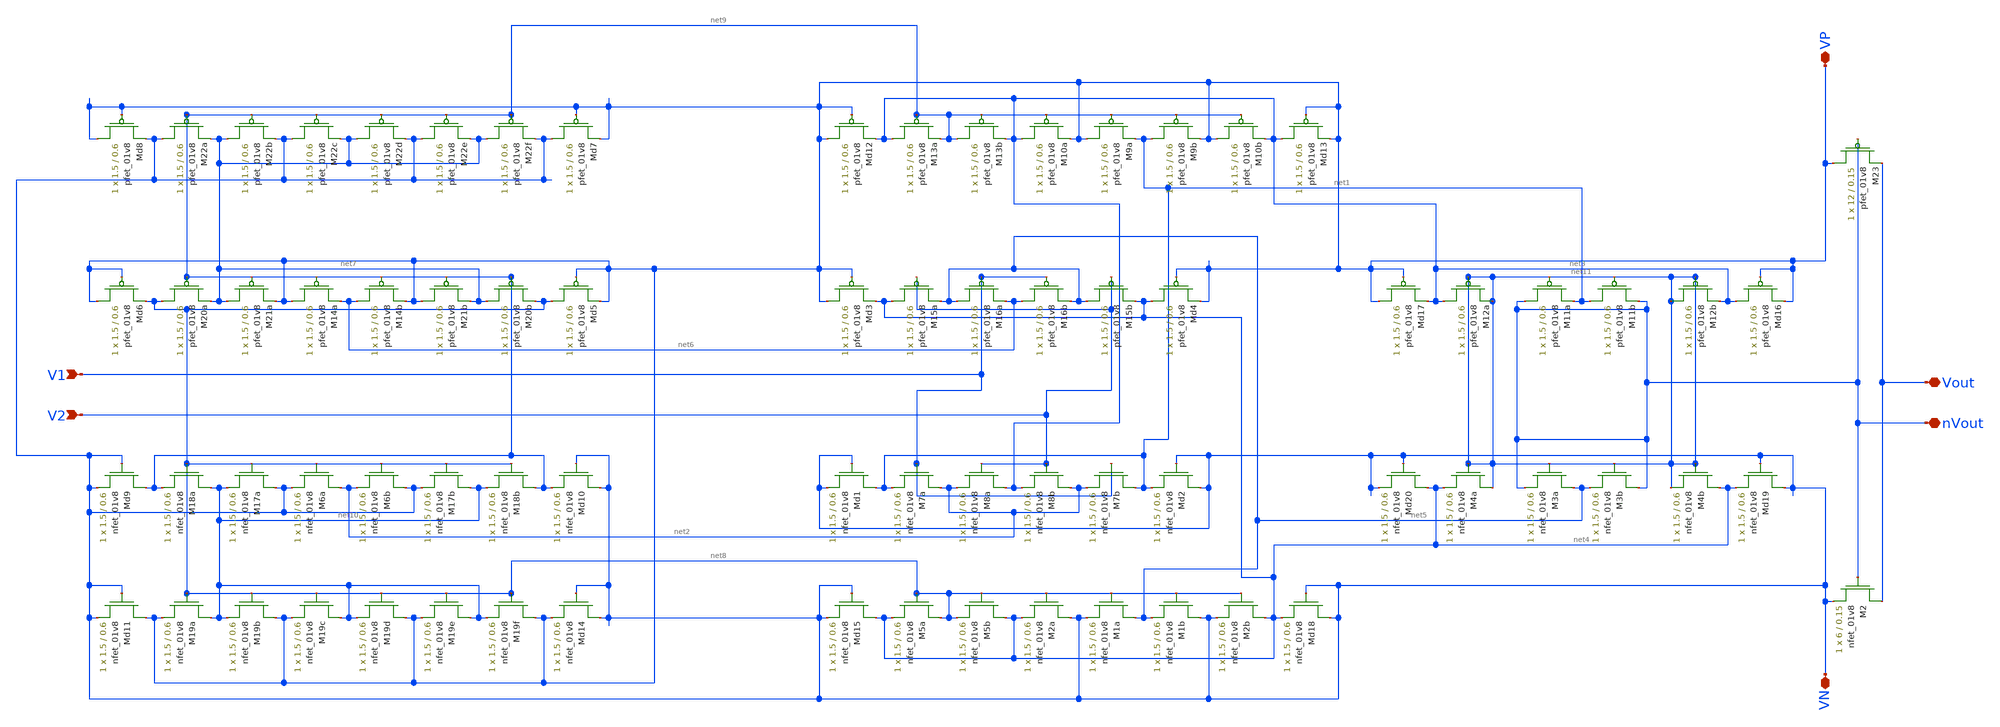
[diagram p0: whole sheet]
** sch_path: analog/sbc2.sch
**.subckt sbc2 V1 V2 Vout nVout VP VN
*.ipin V1
*.ipin V2
*.iopin Vout
*.iopin nVout
*.iopin VP
*.iopin VN
XM7a net2 V1 net1 GND sky130_fd_pr__nfet_01v8 L=0.6 W=1.5 nf=1 ad='int((nf+1)/2) * W/nf * 0.29' as='int((nf+2)/2) * W/nf * 0.29'
+ pd='2*int((nf+1)/2) * (W/nf + 0.29)' ps='2*int((nf+2)/2) * (W/nf + 0.29)' nrd='0.29 / W' nrs='0.29 / W'
+ sa=0 sb=0 sd=0 mult=1 m=1
XM8a net3 V2 net2 GND sky130_fd_pr__nfet_01v8 L=0.6 W=1.5 nf=1 ad='int((nf+1)/2) * W/nf * 0.29' as='int((nf+2)/2) * W/nf * 0.29'
+ pd='2*int((nf+1)/2) * (W/nf + 0.29)' ps='2*int((nf+2)/2) * (W/nf + 0.29)' nrd='0.29 / W' nrs='0.29 / W'
+ sa=0 sb=0 sd=0 mult=1 m=1
XM8b net2 V2 net3 GND sky130_fd_pr__nfet_01v8 L=0.6 W=1.5 nf=1 ad='int((nf+1)/2) * W/nf * 0.29' as='int((nf+2)/2) * W/nf * 0.29'
+ pd='2*int((nf+1)/2) * (W/nf + 0.29)' ps='2*int((nf+2)/2) * (W/nf + 0.29)' nrd='0.29 / W' nrs='0.29 / W'
+ sa=0 sb=0 sd=0 mult=1 m=1
XM7b net1 V1 net2 GND sky130_fd_pr__nfet_01v8 L=0.6 W=1.5 nf=1 ad='int((nf+1)/2) * W/nf * 0.29' as='int((nf+2)/2) * W/nf * 0.29'
+ pd='2*int((nf+1)/2) * (W/nf + 0.29)' ps='2*int((nf+2)/2) * (W/nf + 0.29)' nrd='0.29 / W' nrs='0.29 / W'
+ sa=0 sb=0 sd=0 mult=1 m=1
XMd1 net1 VN VN GND sky130_fd_pr__nfet_01v8 L=0.6 W=1.5 nf=1 ad='int((nf+1)/2) * W/nf * 0.29' as='int((nf+2)/2) * W/nf * 0.29'
+ pd='2*int((nf+1)/2) * (W/nf + 0.29)' ps='2*int((nf+2)/2) * (W/nf + 0.29)' nrd='0.29 / W' nrs='0.29 / W'
+ sa=0 sb=0 sd=0 mult=1 m=1
XMd2 VN VN net1 GND sky130_fd_pr__nfet_01v8 L=0.6 W=1.5 nf=1 ad='int((nf+1)/2) * W/nf * 0.29' as='int((nf+2)/2) * W/nf * 0.29'
+ pd='2*int((nf+1)/2) * (W/nf + 0.29)' ps='2*int((nf+2)/2) * (W/nf + 0.29)' nrd='0.29 / W' nrs='0.29 / W'
+ sa=0 sb=0 sd=0 mult=1 m=1
XMd3 VP VP net4 VDD sky130_fd_pr__pfet_01v8 L=0.6 W=1.5 nf=1 ad='int((nf+1)/2) * W/nf * 0.29' as='int((nf+2)/2) * W/nf * 0.29'
+ pd='2*int((nf+1)/2) * (W/nf + 0.29)' ps='2*int((nf+2)/2) * (W/nf + 0.29)' nrd='0.29 / W' nrs='0.29 / W'
+ sa=0 sb=0 sd=0 mult=1 m=1
XM15a net4 V2 net5 VDD sky130_fd_pr__pfet_01v8 L=0.6 W=1.5 nf=1 ad='int((nf+1)/2) * W/nf * 0.29' as='int((nf+2)/2) * W/nf * 0.29'
+ pd='2*int((nf+1)/2) * (W/nf + 0.29)' ps='2*int((nf+2)/2) * (W/nf + 0.29)' nrd='0.29 / W' nrs='0.29 / W'
+ sa=0 sb=0 sd=0 mult=1 m=1
XM16a net5 V1 net6 VDD sky130_fd_pr__pfet_01v8 L=0.6 W=1.5 nf=1 ad='int((nf+1)/2) * W/nf * 0.29' as='int((nf+2)/2) * W/nf * 0.29'
+ pd='2*int((nf+1)/2) * (W/nf + 0.29)' ps='2*int((nf+2)/2) * (W/nf + 0.29)' nrd='0.29 / W' nrs='0.29 / W'
+ sa=0 sb=0 sd=0 mult=1 m=1
XM16b net6 V1 net5 VDD sky130_fd_pr__pfet_01v8 L=0.6 W=1.5 nf=1 ad='int((nf+1)/2) * W/nf * 0.29' as='int((nf+2)/2) * W/nf * 0.29'
+ pd='2*int((nf+1)/2) * (W/nf + 0.29)' ps='2*int((nf+2)/2) * (W/nf + 0.29)' nrd='0.29 / W' nrs='0.29 / W'
+ sa=0 sb=0 sd=0 mult=1 m=1
XM15b net5 V2 net4 VDD sky130_fd_pr__pfet_01v8 L=0.6 W=1.5 nf=1 ad='int((nf+1)/2) * W/nf * 0.29' as='int((nf+2)/2) * W/nf * 0.29'
+ pd='2*int((nf+1)/2) * (W/nf + 0.29)' ps='2*int((nf+2)/2) * (W/nf + 0.29)' nrd='0.29 / W' nrs='0.29 / W'
+ sa=0 sb=0 sd=0 mult=1 m=1
XMd4 net4 VP VP VDD sky130_fd_pr__pfet_01v8 L=0.6 W=1.5 nf=1 ad='int((nf+1)/2) * W/nf * 0.29' as='int((nf+2)/2) * W/nf * 0.29'
+ pd='2*int((nf+1)/2) * (W/nf + 0.29)' ps='2*int((nf+2)/2) * (W/nf + 0.29)' nrd='0.29 / W' nrs='0.29 / W'
+ sa=0 sb=0 sd=0 mult=1 m=1
XM20a net8 net9 net7 VDD sky130_fd_pr__pfet_01v8 L=0.6 W=1.5 nf=1 ad='int((nf+1)/2) * W/nf * 0.29' as='int((nf+2)/2) * W/nf * 0.29'
+ pd='2*int((nf+1)/2) * (W/nf + 0.29)' ps='2*int((nf+2)/2) * (W/nf + 0.29)' nrd='0.29 / W' nrs='0.29 / W'
+ sa=0 sb=0 sd=0 mult=1 m=1
XM21a net7 net9 VP VDD sky130_fd_pr__pfet_01v8 L=0.6 W=1.5 nf=1 ad='int((nf+1)/2) * W/nf * 0.29' as='int((nf+2)/2) * W/nf * 0.29'
+ pd='2*int((nf+1)/2) * (W/nf + 0.29)' ps='2*int((nf+2)/2) * (W/nf + 0.29)' nrd='0.29 / W' nrs='0.29 / W'
+ sa=0 sb=0 sd=0 mult=1 m=1
XM14a VP net9 net6 VDD sky130_fd_pr__pfet_01v8 L=0.6 W=1.5 nf=1 ad='int((nf+1)/2) * W/nf * 0.29' as='int((nf+2)/2) * W/nf * 0.29'
+ pd='2*int((nf+1)/2) * (W/nf + 0.29)' ps='2*int((nf+2)/2) * (W/nf + 0.29)' nrd='0.29 / W' nrs='0.29 / W'
+ sa=0 sb=0 sd=0 mult=1 m=1
XM14b net6 net9 VP VDD sky130_fd_pr__pfet_01v8 L=0.6 W=1.5 nf=1 ad='int((nf+1)/2) * W/nf * 0.29' as='int((nf+2)/2) * W/nf * 0.29'
+ pd='2*int((nf+1)/2) * (W/nf + 0.29)' ps='2*int((nf+2)/2) * (W/nf + 0.29)' nrd='0.29 / W' nrs='0.29 / W'
+ sa=0 sb=0 sd=0 mult=1 m=1
XM21b VP net9 net7 VDD sky130_fd_pr__pfet_01v8 L=0.6 W=1.5 nf=1 ad='int((nf+1)/2) * W/nf * 0.29' as='int((nf+2)/2) * W/nf * 0.29'
+ pd='2*int((nf+1)/2) * (W/nf + 0.29)' ps='2*int((nf+2)/2) * (W/nf + 0.29)' nrd='0.29 / W' nrs='0.29 / W'
+ sa=0 sb=0 sd=0 mult=1 m=1
XM20b net7 net9 net8 VDD sky130_fd_pr__pfet_01v8 L=0.6 W=1.5 nf=1 ad='int((nf+1)/2) * W/nf * 0.29' as='int((nf+2)/2) * W/nf * 0.29'
+ pd='2*int((nf+1)/2) * (W/nf + 0.29)' ps='2*int((nf+2)/2) * (W/nf + 0.29)' nrd='0.29 / W' nrs='0.29 / W'
+ sa=0 sb=0 sd=0 mult=1 m=1
XMd5 net8 VP VP VDD sky130_fd_pr__pfet_01v8 L=0.6 W=1.5 nf=1 ad='int((nf+1)/2) * W/nf * 0.29' as='int((nf+2)/2) * W/nf * 0.29'
+ pd='2*int((nf+1)/2) * (W/nf + 0.29)' ps='2*int((nf+2)/2) * (W/nf + 0.29)' nrd='0.29 / W' nrs='0.29 / W'
+ sa=0 sb=0 sd=0 mult=1 m=1
XMd6 VP VP net8 VDD sky130_fd_pr__pfet_01v8 L=0.6 W=1.5 nf=1 ad='int((nf+1)/2) * W/nf * 0.29' as='int((nf+2)/2) * W/nf * 0.29'
+ pd='2*int((nf+1)/2) * (W/nf + 0.29)' ps='2*int((nf+2)/2) * (W/nf + 0.29)' nrd='0.29 / W' nrs='0.29 / W'
+ sa=0 sb=0 sd=0 mult=1 m=1
XM22a VN net9 net7 VDD sky130_fd_pr__pfet_01v8 L=0.6 W=1.5 nf=1 ad='int((nf+1)/2) * W/nf * 0.29' as='int((nf+2)/2) * W/nf * 0.29'
+ pd='2*int((nf+1)/2) * (W/nf + 0.29)' ps='2*int((nf+2)/2) * (W/nf + 0.29)' nrd='0.29 / W' nrs='0.29 / W'
+ sa=0 sb=0 sd=0 mult=1 m=1
XM22b net7 net9 VN VDD sky130_fd_pr__pfet_01v8 L=0.6 W=1.5 nf=1 ad='int((nf+1)/2) * W/nf * 0.29' as='int((nf+2)/2) * W/nf * 0.29'
+ pd='2*int((nf+1)/2) * (W/nf + 0.29)' ps='2*int((nf+2)/2) * (W/nf + 0.29)' nrd='0.29 / W' nrs='0.29 / W'
+ sa=0 sb=0 sd=0 mult=1 m=1
XM22c VN net9 net7 VDD sky130_fd_pr__pfet_01v8 L=0.6 W=1.5 nf=1 ad='int((nf+1)/2) * W/nf * 0.29' as='int((nf+2)/2) * W/nf * 0.29'
+ pd='2*int((nf+1)/2) * (W/nf + 0.29)' ps='2*int((nf+2)/2) * (W/nf + 0.29)' nrd='0.29 / W' nrs='0.29 / W'
+ sa=0 sb=0 sd=0 mult=1 m=1
XM22d net7 net9 VN VDD sky130_fd_pr__pfet_01v8 L=0.6 W=1.5 nf=1 ad='int((nf+1)/2) * W/nf * 0.29' as='int((nf+2)/2) * W/nf * 0.29'
+ pd='2*int((nf+1)/2) * (W/nf + 0.29)' ps='2*int((nf+2)/2) * (W/nf + 0.29)' nrd='0.29 / W' nrs='0.29 / W'
+ sa=0 sb=0 sd=0 mult=1 m=1
XM22e VN net9 net7 VDD sky130_fd_pr__pfet_01v8 L=0.6 W=1.5 nf=1 ad='int((nf+1)/2) * W/nf * 0.29' as='int((nf+2)/2) * W/nf * 0.29'
+ pd='2*int((nf+1)/2) * (W/nf + 0.29)' ps='2*int((nf+2)/2) * (W/nf + 0.29)' nrd='0.29 / W' nrs='0.29 / W'
+ sa=0 sb=0 sd=0 mult=1 m=1
XM22f net7 net9 VN VDD sky130_fd_pr__pfet_01v8 L=0.6 W=1.5 nf=1 ad='int((nf+1)/2) * W/nf * 0.29' as='int((nf+2)/2) * W/nf * 0.29'
+ pd='2*int((nf+1)/2) * (W/nf + 0.29)' ps='2*int((nf+2)/2) * (W/nf + 0.29)' nrd='0.29 / W' nrs='0.29 / W'
+ sa=0 sb=0 sd=0 mult=1 m=1
XMd7 VN VP VP VDD sky130_fd_pr__pfet_01v8 L=0.6 W=1.5 nf=1 ad='int((nf+1)/2) * W/nf * 0.29' as='int((nf+2)/2) * W/nf * 0.29'
+ pd='2*int((nf+1)/2) * (W/nf + 0.29)' ps='2*int((nf+2)/2) * (W/nf + 0.29)' nrd='0.29 / W' nrs='0.29 / W'
+ sa=0 sb=0 sd=0 mult=1 m=1
XMd8 VP VP VN VDD sky130_fd_pr__pfet_01v8 L=0.6 W=1.5 nf=1 ad='int((nf+1)/2) * W/nf * 0.29' as='int((nf+2)/2) * W/nf * 0.29'
+ pd='2*int((nf+1)/2) * (W/nf + 0.29)' ps='2*int((nf+2)/2) * (W/nf + 0.29)' nrd='0.29 / W' nrs='0.29 / W'
+ sa=0 sb=0 sd=0 mult=1 m=1
XM18a net10 net8 net9 GND sky130_fd_pr__nfet_01v8 L=0.6 W=1.5 nf=1 ad='int((nf+1)/2) * W/nf * 0.29' as='int((nf+2)/2) * W/nf * 0.29'
+ pd='2*int((nf+1)/2) * (W/nf + 0.29)' ps='2*int((nf+2)/2) * (W/nf + 0.29)' nrd='0.29 / W' nrs='0.29 / W'
+ sa=0 sb=0 sd=0 mult=1 m=1
XM17a VN net8 net10 GND sky130_fd_pr__nfet_01v8 L=0.6 W=1.5 nf=1 ad='int((nf+1)/2) * W/nf * 0.29' as='int((nf+2)/2) * W/nf * 0.29'
+ pd='2*int((nf+1)/2) * (W/nf + 0.29)' ps='2*int((nf+2)/2) * (W/nf + 0.29)' nrd='0.29 / W' nrs='0.29 / W'
+ sa=0 sb=0 sd=0 mult=1 m=1
XM6a net2 net8 VN GND sky130_fd_pr__nfet_01v8 L=0.6 W=1.5 nf=1 ad='int((nf+1)/2) * W/nf * 0.29' as='int((nf+2)/2) * W/nf * 0.29'
+ pd='2*int((nf+1)/2) * (W/nf + 0.29)' ps='2*int((nf+2)/2) * (W/nf + 0.29)' nrd='0.29 / W' nrs='0.29 / W'
+ sa=0 sb=0 sd=0 mult=1 m=1
XM6b VN net8 net2 GND sky130_fd_pr__nfet_01v8 L=0.6 W=1.5 nf=1 ad='int((nf+1)/2) * W/nf * 0.29' as='int((nf+2)/2) * W/nf * 0.29'
+ pd='2*int((nf+1)/2) * (W/nf + 0.29)' ps='2*int((nf+2)/2) * (W/nf + 0.29)' nrd='0.29 / W' nrs='0.29 / W'
+ sa=0 sb=0 sd=0 mult=1 m=1
XMd9 net9 VN VN GND sky130_fd_pr__nfet_01v8 L=0.6 W=1.5 nf=1 ad='int((nf+1)/2) * W/nf * 0.29' as='int((nf+2)/2) * W/nf * 0.29'
+ pd='2*int((nf+1)/2) * (W/nf + 0.29)' ps='2*int((nf+2)/2) * (W/nf + 0.29)' nrd='0.29 / W' nrs='0.29 / W'
+ sa=0 sb=0 sd=0 mult=1 m=1
XM17b net10 net8 VN GND sky130_fd_pr__nfet_01v8 L=0.6 W=1.5 nf=1 ad='int((nf+1)/2) * W/nf * 0.29' as='int((nf+2)/2) * W/nf * 0.29'
+ pd='2*int((nf+1)/2) * (W/nf + 0.29)' ps='2*int((nf+2)/2) * (W/nf + 0.29)' nrd='0.29 / W' nrs='0.29 / W'
+ sa=0 sb=0 sd=0 mult=1 m=1
XM18b net9 net8 net10 GND sky130_fd_pr__nfet_01v8 L=0.6 W=1.5 nf=1 ad='int((nf+1)/2) * W/nf * 0.29' as='int((nf+2)/2) * W/nf * 0.29'
+ pd='2*int((nf+1)/2) * (W/nf + 0.29)' ps='2*int((nf+2)/2) * (W/nf + 0.29)' nrd='0.29 / W' nrs='0.29 / W'
+ sa=0 sb=0 sd=0 mult=1 m=1
XMd10 VN VN net9 GND sky130_fd_pr__nfet_01v8 L=0.6 W=1.5 nf=1 ad='int((nf+1)/2) * W/nf * 0.29' as='int((nf+2)/2) * W/nf * 0.29'
+ pd='2*int((nf+1)/2) * (W/nf + 0.29)' ps='2*int((nf+2)/2) * (W/nf + 0.29)' nrd='0.29 / W' nrs='0.29 / W'
+ sa=0 sb=0 sd=0 mult=1 m=1
XM19a net10 net8 VP GND sky130_fd_pr__nfet_01v8 L=0.6 W=1.5 nf=1 ad='int((nf+1)/2) * W/nf * 0.29' as='int((nf+2)/2) * W/nf * 0.29'
+ pd='2*int((nf+1)/2) * (W/nf + 0.29)' ps='2*int((nf+2)/2) * (W/nf + 0.29)' nrd='0.29 / W' nrs='0.29 / W'
+ sa=0 sb=0 sd=0 mult=1 m=1
XM19b VP net8 net10 GND sky130_fd_pr__nfet_01v8 L=0.6 W=1.5 nf=1 ad='int((nf+1)/2) * W/nf * 0.29' as='int((nf+2)/2) * W/nf * 0.29'
+ pd='2*int((nf+1)/2) * (W/nf + 0.29)' ps='2*int((nf+2)/2) * (W/nf + 0.29)' nrd='0.29 / W' nrs='0.29 / W'
+ sa=0 sb=0 sd=0 mult=1 m=1
XM19c net10 net8 VP GND sky130_fd_pr__nfet_01v8 L=0.6 W=1.5 nf=1 ad='int((nf+1)/2) * W/nf * 0.29' as='int((nf+2)/2) * W/nf * 0.29'
+ pd='2*int((nf+1)/2) * (W/nf + 0.29)' ps='2*int((nf+2)/2) * (W/nf + 0.29)' nrd='0.29 / W' nrs='0.29 / W'
+ sa=0 sb=0 sd=0 mult=1 m=1
XM19d VP net8 net10 GND sky130_fd_pr__nfet_01v8 L=0.6 W=1.5 nf=1 ad='int((nf+1)/2) * W/nf * 0.29' as='int((nf+2)/2) * W/nf * 0.29'
+ pd='2*int((nf+1)/2) * (W/nf + 0.29)' ps='2*int((nf+2)/2) * (W/nf + 0.29)' nrd='0.29 / W' nrs='0.29 / W'
+ sa=0 sb=0 sd=0 mult=1 m=1
XMd11 VP VN VN GND sky130_fd_pr__nfet_01v8 L=0.6 W=1.5 nf=1 ad='int((nf+1)/2) * W/nf * 0.29' as='int((nf+2)/2) * W/nf * 0.29'
+ pd='2*int((nf+1)/2) * (W/nf + 0.29)' ps='2*int((nf+2)/2) * (W/nf + 0.29)' nrd='0.29 / W' nrs='0.29 / W'
+ sa=0 sb=0 sd=0 mult=1 m=1
XM19e net10 net8 VP GND sky130_fd_pr__nfet_01v8 L=0.6 W=1.5 nf=1 ad='int((nf+1)/2) * W/nf * 0.29' as='int((nf+2)/2) * W/nf * 0.29'
+ pd='2*int((nf+1)/2) * (W/nf + 0.29)' ps='2*int((nf+2)/2) * (W/nf + 0.29)' nrd='0.29 / W' nrs='0.29 / W'
+ sa=0 sb=0 sd=0 mult=1 m=1
XM19f VP net8 net10 GND sky130_fd_pr__nfet_01v8 L=0.6 W=1.5 nf=1 ad='int((nf+1)/2) * W/nf * 0.29' as='int((nf+2)/2) * W/nf * 0.29'
+ pd='2*int((nf+1)/2) * (W/nf + 0.29)' ps='2*int((nf+2)/2) * (W/nf + 0.29)' nrd='0.29 / W' nrs='0.29 / W'
+ sa=0 sb=0 sd=0 mult=1 m=1
XMd14 VN VN VP GND sky130_fd_pr__nfet_01v8 L=0.6 W=1.5 nf=1 ad='int((nf+1)/2) * W/nf * 0.29' as='int((nf+2)/2) * W/nf * 0.29'
+ pd='2*int((nf+1)/2) * (W/nf + 0.29)' ps='2*int((nf+2)/2) * (W/nf + 0.29)' nrd='0.29 / W' nrs='0.29 / W'
+ sa=0 sb=0 sd=0 mult=1 m=1
XM13a net3 net9 net9 VDD sky130_fd_pr__pfet_01v8 L=0.6 W=1.5 nf=1 ad='int((nf+1)/2) * W/nf * 0.29' as='int((nf+2)/2) * W/nf * 0.29'
+ pd='2*int((nf+1)/2) * (W/nf + 0.29)' ps='2*int((nf+2)/2) * (W/nf + 0.29)' nrd='0.29 / W' nrs='0.29 / W'
+ sa=0 sb=0 sd=0 mult=1 m=1
XM13b net9 net9 net3 VDD sky130_fd_pr__pfet_01v8 L=0.6 W=1.5 nf=1 ad='int((nf+1)/2) * W/nf * 0.29' as='int((nf+2)/2) * W/nf * 0.29'
+ pd='2*int((nf+1)/2) * (W/nf + 0.29)' ps='2*int((nf+2)/2) * (W/nf + 0.29)' nrd='0.29 / W' nrs='0.29 / W'
+ sa=0 sb=0 sd=0 mult=1 m=1
XM10a net3 net9 VP VDD sky130_fd_pr__pfet_01v8 L=0.6 W=1.5 nf=1 ad='int((nf+1)/2) * W/nf * 0.29' as='int((nf+2)/2) * W/nf * 0.29'
+ pd='2*int((nf+1)/2) * (W/nf + 0.29)' ps='2*int((nf+2)/2) * (W/nf + 0.29)' nrd='0.29 / W' nrs='0.29 / W'
+ sa=0 sb=0 sd=0 mult=1 m=1
XM9a VP net9 net1 VDD sky130_fd_pr__pfet_01v8 L=0.6 W=1.5 nf=1 ad='int((nf+1)/2) * W/nf * 0.29' as='int((nf+2)/2) * W/nf * 0.29'
+ pd='2*int((nf+1)/2) * (W/nf + 0.29)' ps='2*int((nf+2)/2) * (W/nf + 0.29)' nrd='0.29 / W' nrs='0.29 / W'
+ sa=0 sb=0 sd=0 mult=1 m=1
XM9b net1 net9 VP VDD sky130_fd_pr__pfet_01v8 L=0.6 W=1.5 nf=1 ad='int((nf+1)/2) * W/nf * 0.29' as='int((nf+2)/2) * W/nf * 0.29'
+ pd='2*int((nf+1)/2) * (W/nf + 0.29)' ps='2*int((nf+2)/2) * (W/nf + 0.29)' nrd='0.29 / W' nrs='0.29 / W'
+ sa=0 sb=0 sd=0 mult=1 m=1
XM10b VP net9 net3 VDD sky130_fd_pr__pfet_01v8 L=0.6 W=1.5 nf=1 ad='int((nf+1)/2) * W/nf * 0.29' as='int((nf+2)/2) * W/nf * 0.29'
+ pd='2*int((nf+1)/2) * (W/nf + 0.29)' ps='2*int((nf+2)/2) * (W/nf + 0.29)' nrd='0.29 / W' nrs='0.29 / W'
+ sa=0 sb=0 sd=0 mult=1 m=1
XMd12 VP VP net3 VDD sky130_fd_pr__pfet_01v8 L=0.6 W=1.5 nf=1 ad='int((nf+1)/2) * W/nf * 0.29' as='int((nf+2)/2) * W/nf * 0.29'
+ pd='2*int((nf+1)/2) * (W/nf + 0.29)' ps='2*int((nf+2)/2) * (W/nf + 0.29)' nrd='0.29 / W' nrs='0.29 / W'
+ sa=0 sb=0 sd=0 mult=1 m=1
XMd13 net3 VP VP VDD sky130_fd_pr__pfet_01v8 L=0.6 W=1.5 nf=1 ad='int((nf+1)/2) * W/nf * 0.29' as='int((nf+2)/2) * W/nf * 0.29'
+ pd='2*int((nf+1)/2) * (W/nf + 0.29)' ps='2*int((nf+2)/2) * (W/nf + 0.29)' nrd='0.29 / W' nrs='0.29 / W'
+ sa=0 sb=0 sd=0 mult=1 m=1
XM5a net8 net8 net4 GND sky130_fd_pr__nfet_01v8 L=0.6 W=1.5 nf=1 ad='int((nf+1)/2) * W/nf * 0.29' as='int((nf+2)/2) * W/nf * 0.29'
+ pd='2*int((nf+1)/2) * (W/nf + 0.29)' ps='2*int((nf+2)/2) * (W/nf + 0.29)' nrd='0.29 / W' nrs='0.29 / W'
+ sa=0 sb=0 sd=0 mult=1 m=1
XM5b net4 net8 net8 GND sky130_fd_pr__nfet_01v8 L=0.6 W=1.5 nf=1 ad='int((nf+1)/2) * W/nf * 0.29' as='int((nf+2)/2) * W/nf * 0.29'
+ pd='2*int((nf+1)/2) * (W/nf + 0.29)' ps='2*int((nf+2)/2) * (W/nf + 0.29)' nrd='0.29 / W' nrs='0.29 / W'
+ sa=0 sb=0 sd=0 mult=1 m=1
XM2a VN net8 net4 GND sky130_fd_pr__nfet_01v8 L=0.6 W=1.5 nf=1 ad='int((nf+1)/2) * W/nf * 0.29' as='int((nf+2)/2) * W/nf * 0.29'
+ pd='2*int((nf+1)/2) * (W/nf + 0.29)' ps='2*int((nf+2)/2) * (W/nf + 0.29)' nrd='0.29 / W' nrs='0.29 / W'
+ sa=0 sb=0 sd=0 mult=1 m=1
XM1a net5 net8 VN GND sky130_fd_pr__nfet_01v8 L=0.6 W=1.5 nf=1 ad='int((nf+1)/2) * W/nf * 0.29' as='int((nf+2)/2) * W/nf * 0.29'
+ pd='2*int((nf+1)/2) * (W/nf + 0.29)' ps='2*int((nf+2)/2) * (W/nf + 0.29)' nrd='0.29 / W' nrs='0.29 / W'
+ sa=0 sb=0 sd=0 mult=1 m=1
XMd15 net4 VN VN GND sky130_fd_pr__nfet_01v8 L=0.6 W=1.5 nf=1 ad='int((nf+1)/2) * W/nf * 0.29' as='int((nf+2)/2) * W/nf * 0.29'
+ pd='2*int((nf+1)/2) * (W/nf + 0.29)' ps='2*int((nf+2)/2) * (W/nf + 0.29)' nrd='0.29 / W' nrs='0.29 / W'
+ sa=0 sb=0 sd=0 mult=1 m=1
XM1b VN net8 net5 GND sky130_fd_pr__nfet_01v8 L=0.6 W=1.5 nf=1 ad='int((nf+1)/2) * W/nf * 0.29' as='int((nf+2)/2) * W/nf * 0.29'
+ pd='2*int((nf+1)/2) * (W/nf + 0.29)' ps='2*int((nf+2)/2) * (W/nf + 0.29)' nrd='0.29 / W' nrs='0.29 / W'
+ sa=0 sb=0 sd=0 mult=1 m=1
XM2b net4 net8 VN GND sky130_fd_pr__nfet_01v8 L=0.6 W=1.5 nf=1 ad='int((nf+1)/2) * W/nf * 0.29' as='int((nf+2)/2) * W/nf * 0.29'
+ pd='2*int((nf+1)/2) * (W/nf + 0.29)' ps='2*int((nf+2)/2) * (W/nf + 0.29)' nrd='0.29 / W' nrs='0.29 / W'
+ sa=0 sb=0 sd=0 mult=1 m=1
XMd18 VN VN net4 GND sky130_fd_pr__nfet_01v8 L=0.6 W=1.5 nf=1 ad='int((nf+1)/2) * W/nf * 0.29' as='int((nf+2)/2) * W/nf * 0.29'
+ pd='2*int((nf+1)/2) * (W/nf + 0.29)' ps='2*int((nf+2)/2) * (W/nf + 0.29)' nrd='0.29 / W' nrs='0.29 / W'
+ sa=0 sb=0 sd=0 mult=1 m=1
XM12a net3 net11 net11 VDD sky130_fd_pr__pfet_01v8 L=0.6 W=1.5 nf=1 ad='int((nf+1)/2) * W/nf * 0.29'
+ as='int((nf+2)/2) * W/nf * 0.29' pd='2*int((nf+1)/2) * (W/nf + 0.29)' ps='2*int((nf+2)/2) * (W/nf + 0.29)'
+ nrd='0.29 / W' nrs='0.29 / W' sa=0 sb=0 sd=0 mult=1 m=1
XM11a nVout net11 net1 VDD sky130_fd_pr__pfet_01v8 L=0.6 W=1.5 nf=1 ad='int((nf+1)/2) * W/nf * 0.29'
+ as='int((nf+2)/2) * W/nf * 0.29' pd='2*int((nf+1)/2) * (W/nf + 0.29)' ps='2*int((nf+2)/2) * (W/nf + 0.29)'
+ nrd='0.29 / W' nrs='0.29 / W' sa=0 sb=0 sd=0 mult=1 m=1
XM11b net1 net11 nVout VDD sky130_fd_pr__pfet_01v8 L=0.6 W=1.5 nf=1 ad='int((nf+1)/2) * W/nf * 0.29'
+ as='int((nf+2)/2) * W/nf * 0.29' pd='2*int((nf+1)/2) * (W/nf + 0.29)' ps='2*int((nf+2)/2) * (W/nf + 0.29)'
+ nrd='0.29 / W' nrs='0.29 / W' sa=0 sb=0 sd=0 mult=1 m=1
XM12b net11 net11 net3 VDD sky130_fd_pr__pfet_01v8 L=0.6 W=1.5 nf=1 ad='int((nf+1)/2) * W/nf * 0.29'
+ as='int((nf+2)/2) * W/nf * 0.29' pd='2*int((nf+1)/2) * (W/nf + 0.29)' ps='2*int((nf+2)/2) * (W/nf + 0.29)'
+ nrd='0.29 / W' nrs='0.29 / W' sa=0 sb=0 sd=0 mult=1 m=1
XMd16 net3 VP VP VDD sky130_fd_pr__pfet_01v8 L=0.6 W=1.5 nf=1 ad='int((nf+1)/2) * W/nf * 0.29' as='int((nf+2)/2) * W/nf * 0.29'
+ pd='2*int((nf+1)/2) * (W/nf + 0.29)' ps='2*int((nf+2)/2) * (W/nf + 0.29)' nrd='0.29 / W' nrs='0.29 / W'
+ sa=0 sb=0 sd=0 mult=1 m=1
XMd17 VP VP net3 VDD sky130_fd_pr__pfet_01v8 L=0.6 W=1.5 nf=1 ad='int((nf+1)/2) * W/nf * 0.29' as='int((nf+2)/2) * W/nf * 0.29'
+ pd='2*int((nf+1)/2) * (W/nf + 0.29)' ps='2*int((nf+2)/2) * (W/nf + 0.29)' nrd='0.29 / W' nrs='0.29 / W'
+ sa=0 sb=0 sd=0 mult=1 m=1
XM3a net5 net11 nVout GND sky130_fd_pr__nfet_01v8 L=0.6 W=1.5 nf=1 ad='int((nf+1)/2) * W/nf * 0.29' as='int((nf+2)/2) * W/nf * 0.29'
+ pd='2*int((nf+1)/2) * (W/nf + 0.29)' ps='2*int((nf+2)/2) * (W/nf + 0.29)' nrd='0.29 / W' nrs='0.29 / W'
+ sa=0 sb=0 sd=0 mult=1 m=1
XM4a net11 net11 net4 GND sky130_fd_pr__nfet_01v8 L=0.6 W=1.5 nf=1 ad='int((nf+1)/2) * W/nf * 0.29' as='int((nf+2)/2) * W/nf * 0.29'
+ pd='2*int((nf+1)/2) * (W/nf + 0.29)' ps='2*int((nf+2)/2) * (W/nf + 0.29)' nrd='0.29 / W' nrs='0.29 / W'
+ sa=0 sb=0 sd=0 mult=1 m=1
XM3b nVout net11 net5 GND sky130_fd_pr__nfet_01v8 L=0.6 W=1.5 nf=1 ad='int((nf+1)/2) * W/nf * 0.29' as='int((nf+2)/2) * W/nf * 0.29'
+ pd='2*int((nf+1)/2) * (W/nf + 0.29)' ps='2*int((nf+2)/2) * (W/nf + 0.29)' nrd='0.29 / W' nrs='0.29 / W'
+ sa=0 sb=0 sd=0 mult=1 m=1
XM4b net4 net11 net11 GND sky130_fd_pr__nfet_01v8 L=0.6 W=1.5 nf=1 ad='int((nf+1)/2) * W/nf * 0.29' as='int((nf+2)/2) * W/nf * 0.29'
+ pd='2*int((nf+1)/2) * (W/nf + 0.29)' ps='2*int((nf+2)/2) * (W/nf + 0.29)' nrd='0.29 / W' nrs='0.29 / W'
+ sa=0 sb=0 sd=0 mult=1 m=1
XMd19 VN VN net4 GND sky130_fd_pr__nfet_01v8 L=0.6 W=1.5 nf=1 ad='int((nf+1)/2) * W/nf * 0.29' as='int((nf+2)/2) * W/nf * 0.29'
+ pd='2*int((nf+1)/2) * (W/nf + 0.29)' ps='2*int((nf+2)/2) * (W/nf + 0.29)' nrd='0.29 / W' nrs='0.29 / W'
+ sa=0 sb=0 sd=0 mult=1 m=1
XMd20 net4 VN VN GND sky130_fd_pr__nfet_01v8 L=0.6 W=1.5 nf=1 ad='int((nf+1)/2) * W/nf * 0.29' as='int((nf+2)/2) * W/nf * 0.29'
+ pd='2*int((nf+1)/2) * (W/nf + 0.29)' ps='2*int((nf+2)/2) * (W/nf + 0.29)' nrd='0.29 / W' nrs='0.29 / W'
+ sa=0 sb=0 sd=0 mult=1 m=1
XM2 Vout nVout VN GND sky130_fd_pr__nfet_01v8 L=0.15 W=6 nf=1 ad='int((nf+1)/2) * W/nf * 0.29' as='int((nf+2)/2) * W/nf * 0.29'
+ pd='2*int((nf+1)/2) * (W/nf + 0.29)' ps='2*int((nf+2)/2) * (W/nf + 0.29)' nrd='0.29 / W' nrs='0.29 / W'
+ sa=0 sb=0 sd=0 mult=1 m=1
XM23 VP nVout Vout VDD sky130_fd_pr__pfet_01v8 L=0.15 W=12 nf=1 ad='int((nf+1)/2) * W/nf * 0.29' as='int((nf+2)/2) * W/nf * 0.29'
+ pd='2*int((nf+1)/2) * (W/nf + 0.29)' ps='2*int((nf+2)/2) * (W/nf + 0.29)' nrd='0.29 / W' nrs='0.29 / W'
+ sa=0 sb=0 sd=0 mult=1 m=1
**.ends
.end
